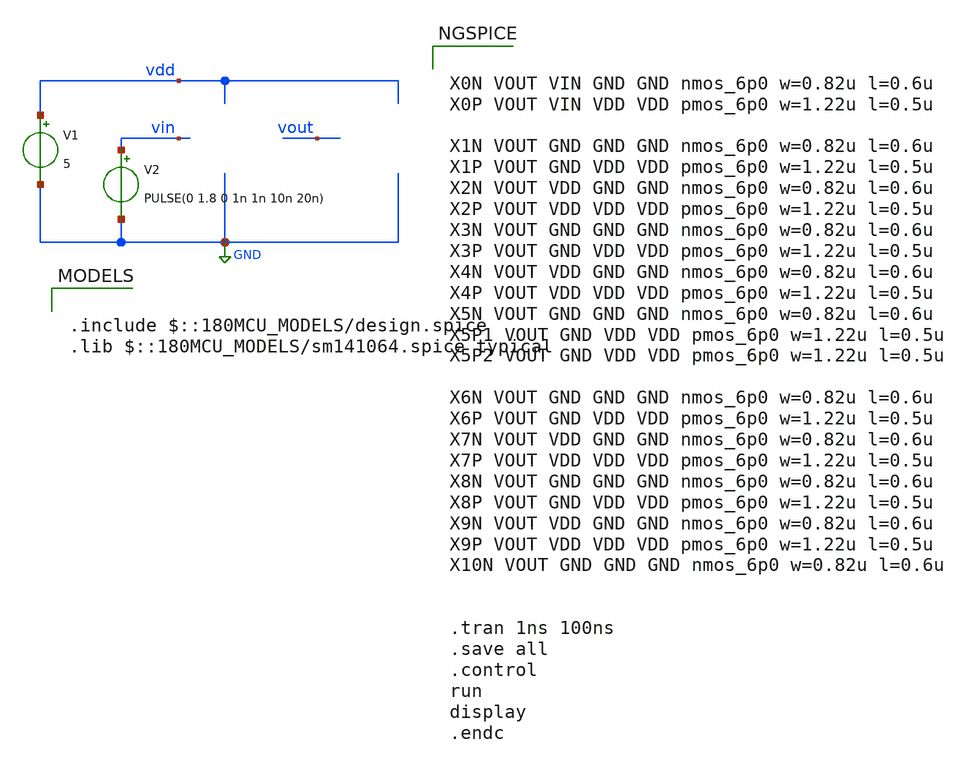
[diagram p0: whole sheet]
** sch_path: xschem/invtest.sch
**.subckt invtest
V1 vdd GND 5
V2 vin GND PULSE(0 1.8 0 1n 1n 10n 20n)
**** begin user architecture code

.include $::180MCU_MODELS/design.spice
.lib $::180MCU_MODELS/sm141064.spice typical



X0N VOUT VIN GND GND nmos_6p0 w=0.82u l=0.6u
X0P VOUT VIN VDD VDD pmos_6p0 w=1.22u l=0.5u

X1N VOUT GND GND GND nmos_6p0 w=0.82u l=0.6u
X1P VOUT GND VDD VDD pmos_6p0 w=1.22u l=0.5u
X2N VOUT VDD GND GND nmos_6p0 w=0.82u l=0.6u
X2P VOUT VDD VDD VDD pmos_6p0 w=1.22u l=0.5u
X3N VOUT GND GND GND nmos_6p0 w=0.82u l=0.6u
X3P VOUT GND VDD VDD pmos_6p0 w=1.22u l=0.5u
X4N VOUT VDD GND GND nmos_6p0 w=0.82u l=0.6u
X4P VOUT VDD VDD VDD pmos_6p0 w=1.22u l=0.5u
X5N VOUT GND GND GND nmos_6p0 w=0.82u l=0.6u
X5P1 VOUT GND VDD VDD pmos_6p0 w=1.22u l=0.5u
X5P2 VOUT GND VDD VDD pmos_6p0 w=1.22u l=0.5u

X6N VOUT GND GND GND nmos_6p0 w=0.82u l=0.6u
X6P VOUT GND VDD VDD pmos_6p0 w=1.22u l=0.5u
X7N VOUT VDD GND GND nmos_6p0 w=0.82u l=0.6u
X7P VOUT VDD VDD VDD pmos_6p0 w=1.22u l=0.5u
X8N VOUT GND GND GND nmos_6p0 w=0.82u l=0.6u
X8P VOUT GND VDD VDD pmos_6p0 w=1.22u l=0.5u
X9N VOUT VDD GND GND nmos_6p0 w=0.82u l=0.6u
X9P VOUT VDD VDD VDD pmos_6p0 w=1.22u l=0.5u
X10N VOUT GND GND GND nmos_6p0 w=0.82u l=0.6u


.tran 1ns 100ns
.save all
.control
run
display
.endc


**** end user architecture code
**.ends
.GLOBAL GND
.end
